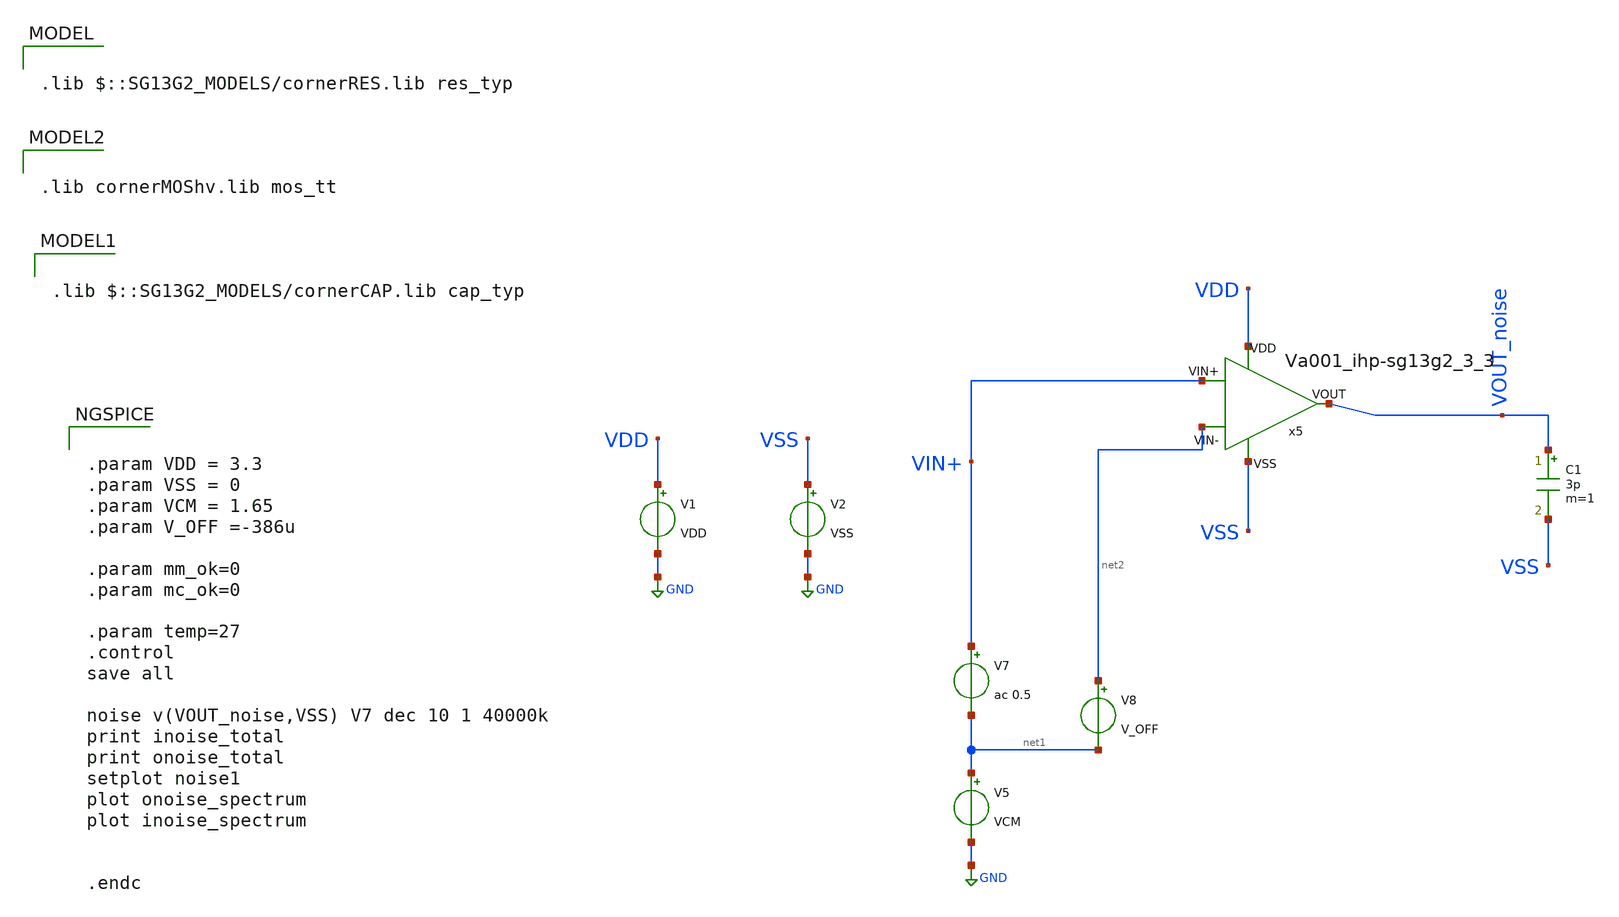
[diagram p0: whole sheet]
** sch_path: Learning/single_ended_amplifiers/VA001_series/Design_and_Analysis_of_Two-Stage_CMOS_Operational_Amplifier_for_Fluorescence_Signal_Processing_ihp130_1_2V/amplifier_design/noise.sch
**.subckt noise
V5 net1 GND VCM
V7 VIN+ net1 ac 0.5
V8 net2 net1 V_OFF
C1 VOUT_noise VSS 3p m=1
x5 VDD VSS net2 VIN+ VOUT_noise Va001_ihp-sg13g2_3_3
V1 VDD GND VDD
V2 VSS GND VSS
**** begin user architecture code

.lib $::SG13G2_MODELS/cornerRES.lib res_typ


.lib cornerMOShv.lib mos_tt


.lib $::SG13G2_MODELS/cornerCAP.lib cap_typ

**** end user architecture code
**.ends

* expanding   symbol:  ihp-sg13g2/Amplifiers/Va001_ihp-sg13g2_3_3.sym # of pins=5
** sym_path: LIB/ihp-sg13g2/Amplifiers/Va001_ihp-sg13g2_3_3.sym
** sch_path: LIB/ihp-sg13g2/Amplifiers/Va001_ihp-sg13g2_3_3.sch
.subckt Va001_ihp-sg13g2_3_3 VDD VSS VIN- VIN+ VOUT
*.iopin VDD
*.iopin VSS
*.iopin VIN-
*.iopin VIN+
*.iopin VOUT
XM2 VB1 VB1 VDD VDD sg13_hv_pmos w=1.5u l=2u ng=2 m=2 mm_ok=1
XM1 VB2 VB1 VDD VDD sg13_hv_pmos w=1.5u l=2u ng=2 m=2 mm_ok=1
XM3 VB1 VB2 net3 VSS sg13_hv_nmos w=1.0u l=2u ng=2 m=2 mm_ok=1
XM4 VB2 VB2 net1 VSS sg13_hv_nmos w=1.0u l=2u ng=2 m=2 mm_ok=1
XM5 net3 net1 net2 VSS sg13_hv_nmos w=2u l=2u ng=2 m=8 mm_ok=1
XM6 net1 net1 VSS VSS sg13_hv_nmos w=2u l=2u ng=2 m=2 mm_ok=1
XR1 net2 VSS sub! rhigh w=0.5e-6 l=5.9e-6 m=1 b=0 mm_ok=1
XM7 net4 VB1 VDD VDD sg13_hv_pmos w=1.5u l=2u ng=2 m=8 mm_ok=1
XM9 net6 VIN+ net4 net4 sg13_hv_pmos w=8u l=0.8u ng=4 m=4 mm_ok=1
XM8 net5 VIN- net4 net4 sg13_hv_pmos w=8u l=0.8u ng=4 m=4 mm_ok=1
XM10 net5 net5 VSS VSS sg13_hv_nmos w=2u l=2u ng=2 m=2 mm_ok=1
XM11 net6 net5 VSS VSS sg13_hv_nmos w=2u l=2u ng=2 m=2 mm_ok=1
XM12 VOUT VB1 VDD VDD sg13_hv_pmos w=1.5u l=2u ng=2 m=16 mm_ok=1
XM13 VOUT net6 VSS VSS sg13_hv_nmos w=2u l=0.8u ng=2 m=4 mm_ok=1
XM14 net6 VB2 net7 VSS sg13_hv_nmos w=2u l=2.7u ng=1 m=2 mm_ok=1
XC1 VOUT net7 cap_cmim w=9e-6 l=9e-6 m=4 mm_ok=1
.ends

.GLOBAL GND
**** begin user architecture code


.param VDD = 3.3
.param VSS = 0
.param VCM = 1.65
.param V_OFF =-386u

.param mm_ok=0
.param mc_ok=0

.param temp=27
.control
save all

noise v(VOUT_noise,VSS) V7 dec 10 1 40000k
print inoise_total
print onoise_total
setplot noise1
plot onoise_spectrum
plot inoise_spectrum


.endc


**** end user architecture code
.end
